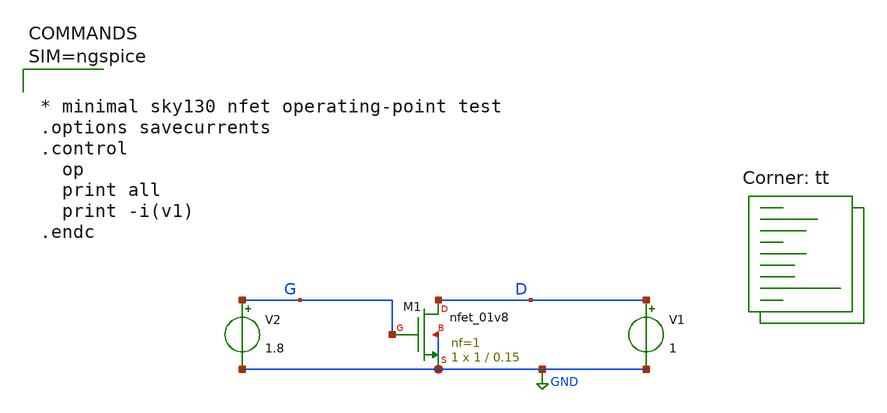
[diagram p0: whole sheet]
** sch_path: sky130A/xschem_libs/sky130_tests/nfet_test_claude/schematic/nfet_test_claude.sch
**.subckt nfet_test_claude
XM1 D G GND GND sky130_fd_pr__nfet_01v8 L=0.15 W=1 nf=1 ad='int((1 + 1)/2) * 1 / 1 * 0.29' as='int((1 + 2)/2) * 1 / 1 * 0.29'
+ pd='2*int((1 + 1)/2) * (1 / 1 + 0.29)' ps='2*int((1 + 2)/2) * (1 / 1 + 0.29)' nrd='0.29 / 1 ' nrs='0.29 / 1 '
+ sa=0 sb=0 sd=0 mult=1 m=1
V1 D GND 1
V2 G GND 1.8
**** begin user architecture code
.lib $::SKYWATER_MODELS/sky130.lib.spice tt



* minimal sky130 nfet operating-point test
.options savecurrents
.control
  op
  print all
  print -i(v1)
.endc



**** end user architecture code
**.ends
.GLOBAL GND
.end
